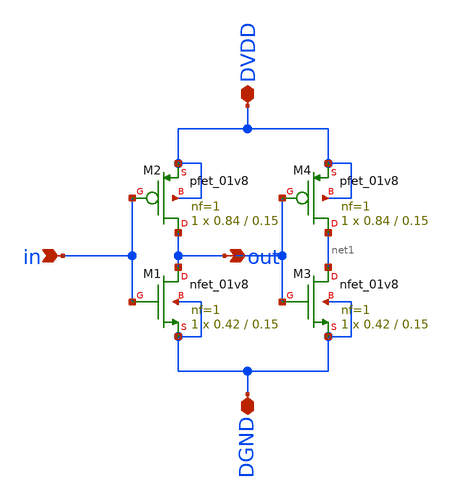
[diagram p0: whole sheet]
** sch_path: tutorial_6/6_1b/inv.sch
**.subckt inv in DVDD DGND out
*.ipin in
*.iopin DVDD
*.iopin DGND
*.opin out
XM1 out in DGND DGND sky130_fd_pr__nfet_01v8 L=0.15 W=0.42 nf=1 ad='int((nf+1)/2) * W/nf * 0.29' as='int((nf+2)/2) * W/nf * 0.29'
+ pd='2*int((nf+1)/2) * (W/nf + 0.29)' ps='2*int((nf+2)/2) * (W/nf + 0.29)' nrd='0.29 / W' nrs='0.29 / W'
+ sa=0 sb=0 sd=0 mult=1 m=1
XM2 out in DVDD DVDD sky130_fd_pr__pfet_01v8 L=0.15 W=0.84 nf=1 ad='int((nf+1)/2) * W/nf * 0.29' as='int((nf+2)/2) * W/nf * 0.29'
+ pd='2*int((nf+1)/2) * (W/nf + 0.29)' ps='2*int((nf+2)/2) * (W/nf + 0.29)' nrd='0.29 / W' nrs='0.29 / W'
+ sa=0 sb=0 sd=0 mult=1 m=1
XM3 net1 out DGND DGND sky130_fd_pr__nfet_01v8 L=0.15 W=0.42 nf=1 ad='int((nf+1)/2) * W/nf * 0.29' as='int((nf+2)/2) * W/nf * 0.29'
+ pd='2*int((nf+1)/2) * (W/nf + 0.29)' ps='2*int((nf+2)/2) * (W/nf + 0.29)' nrd='0.29 / W' nrs='0.29 / W'
+ sa=0 sb=0 sd=0 mult=1 m=1
XM4 net1 out DVDD DVDD sky130_fd_pr__pfet_01v8 L=0.15 W=0.84 nf=1 ad='int((nf+1)/2) * W/nf * 0.29' as='int((nf+2)/2) * W/nf * 0.29'
+ pd='2*int((nf+1)/2) * (W/nf + 0.29)' ps='2*int((nf+2)/2) * (W/nf + 0.29)' nrd='0.29 / W' nrs='0.29 / W'
+ sa=0 sb=0 sd=0 mult=1 m=1
**.ends
.end
